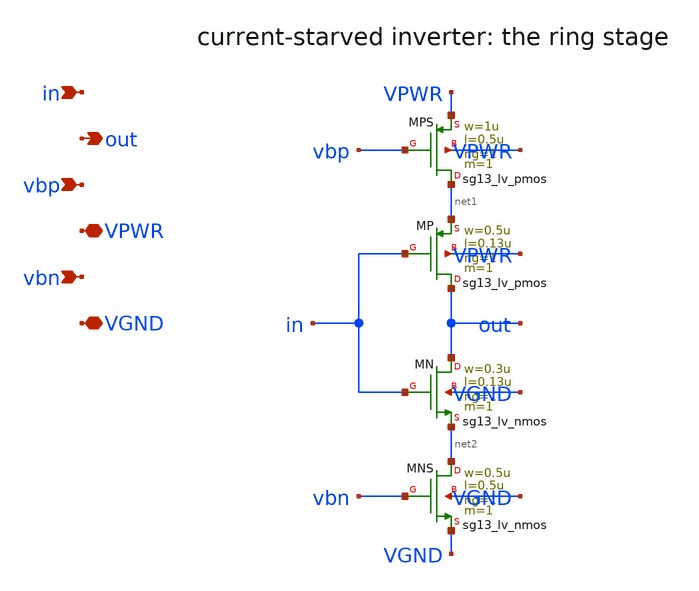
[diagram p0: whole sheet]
** sch_path: analog/xschem/csro_stage.sch
**.subckt csro_stage in out vbp VPWR vbn VGND
*.ipin in
*.opin out
*.ipin vbp
*.iopin VPWR
*.ipin vbn
*.iopin VGND
XMPS net1 vbp VPWR VPWR sg13_lv_pmos w=1u l=0.5u ng=1 m=1 mm_ok=1
XMP out in net1 VPWR sg13_lv_pmos w=0.5u l=0.13u ng=1 m=1 mm_ok=1
XMN out in net2 VGND sg13_lv_nmos w=0.3u l=0.13u ng=1 m=1 mm_ok=1
XMNS net2 vbn VGND VGND sg13_lv_nmos w=0.5u l=0.5u ng=1 m=1 mm_ok=1
**.ends
.end
